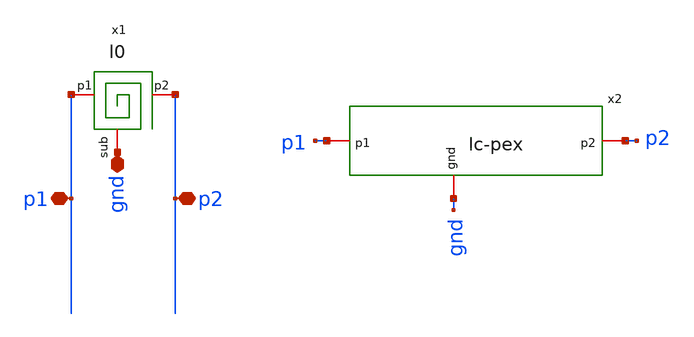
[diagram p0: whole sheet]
** sch_path: examples/sq_1nH_2.5GHz/xschem/lc-pex-full.sch
**.subckt lc-pex-full p1 p2 gnd
*.iopin p1
*.iopin p2
*.iopin gnd
x1 p1 p2 gnd l0
x2 gnd p2 p1 lc-pex
**.ends

* expanding   symbol:  /foss/designs/asitic-example/examples/sq_1nH_2.5GHz/xschem/l0.sym # of pins=3
** sym_path: examples/sq_1nH_2.5GHz/xschem/l0.sym
** sch_path: examples/sq_1nH_2.5GHz/xschem/l0.sch
.subckt l0 p1 p2 sub
*.iopin sub
*.iopin p1
*.iopin p2
R net2 p2 2.857 m=1
L p1 net2 1.006n m=1
Rs1 net1 sub 27.37 m=1
Cs1 p1 net1 33.97f m=1
Cs2 p2 net3 36.78f m=1
Rs2 net3 sub -9 m=1
.ends


* expanding   symbol:  /foss/designs/asitic-example/examples/sq_1nH_2.5GHz/xschem/lc-pex.sym # of
*+ pins=3
** sym_path: examples/sq_1nH_2.5GHz/xschem/lc-pex.sym
** sch_path: examples/sq_1nH_2.5GHz/xschem/lc-pex.sch
.subckt lc-pex gnd p2 p1
*.iopin p1
*.iopin p2
*.iopin gnd
**** begin user architecture code


X0 p1.t0 p2.t3 sky130_fd_pr__cap_mim_m3_2 l=22.3 w=22.3
X1 p1.t1 p2.t2 sky130_fd_pr__cap_mim_m3_2 l=22.3 w=22.3
X2 p1.t2 p2.t1 sky130_fd_pr__cap_mim_m3_2 l=22.3 w=22.3
X3 p1.t3 p2.t0 sky130_fd_pr__cap_mim_m3_2 l=22.3 w=22.3
R0 p1.n2 p1.n0 0.348247
R1 p1.n1 p1.t3 0.0780897
R2 p1 p1.n2 0.070689
R3 p1.n0 p1.t1 0.0686501
R4 p1.n2 p1.n1 0.0520717
R5 p1.n0 p1.t2 0.000500104
R6 p1.n1 p1.t0 0.000500104
R7 p2.n0 p2.t3 0.495841
R8 p2.n1 p2.t1 0.49576
R9 p2 p2.n2 0.483229
R10 p2.n2 p2.n1 0.270536
R11 p2.n2 p2.n0 0.144491
R12 p2.n1 p2.t2 0.000906926
R13 p2.n0 p2.t0 0.000825541
C0 p2 p1 0.159p


**** end user architecture code
.ends

.end
